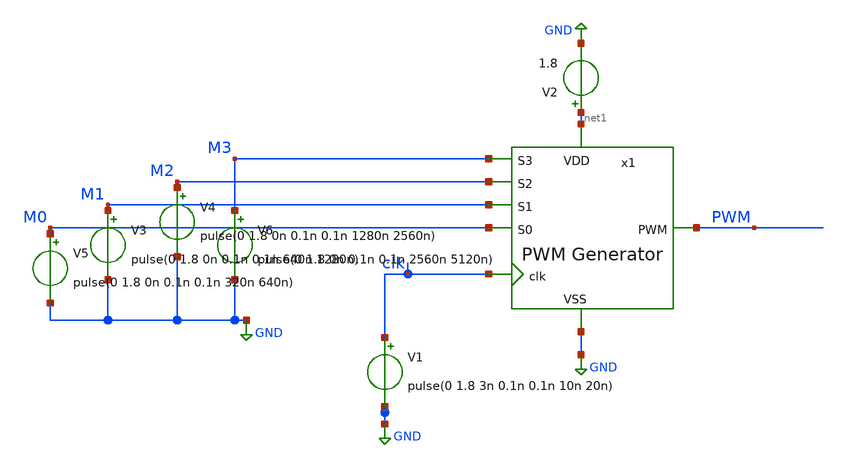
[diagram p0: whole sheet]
** sch_path: Layouts and Schematics/Spice Sim and Schem/pwmtb.sch
**.subckt pwmtb
V1 clk GND pulse(0 1.8 3n 0.1n 0.1n 10n 20n)
V2 net1 GND 1.8
V4 M2 GND pulse(0 1.8 0n 0.1n 0.1n 1280n 2560n)
V3 M1 GND pulse(0 1.8 0n 0.1n 0.1n 640n 1280n)
V5 M0 GND pulse(0 1.8 0n 0.1n 0.1n 320n 640n)
V6 M3 GND pulse(0 1.8 0n 0.1n 0.1n 2560n 5120n)
x1 net1 clk PWM M3 M2 M1 M0 GND pwm
**** begin user architecture code
 .lib $::SKYWATER_MODELS/sky130.lib.spice tt

.include /home/wyatt/EE431
.tran 1n 4800n
.control
run
.endc

**** end user architecture code
**.ends
.GLOBAL GND
.end
